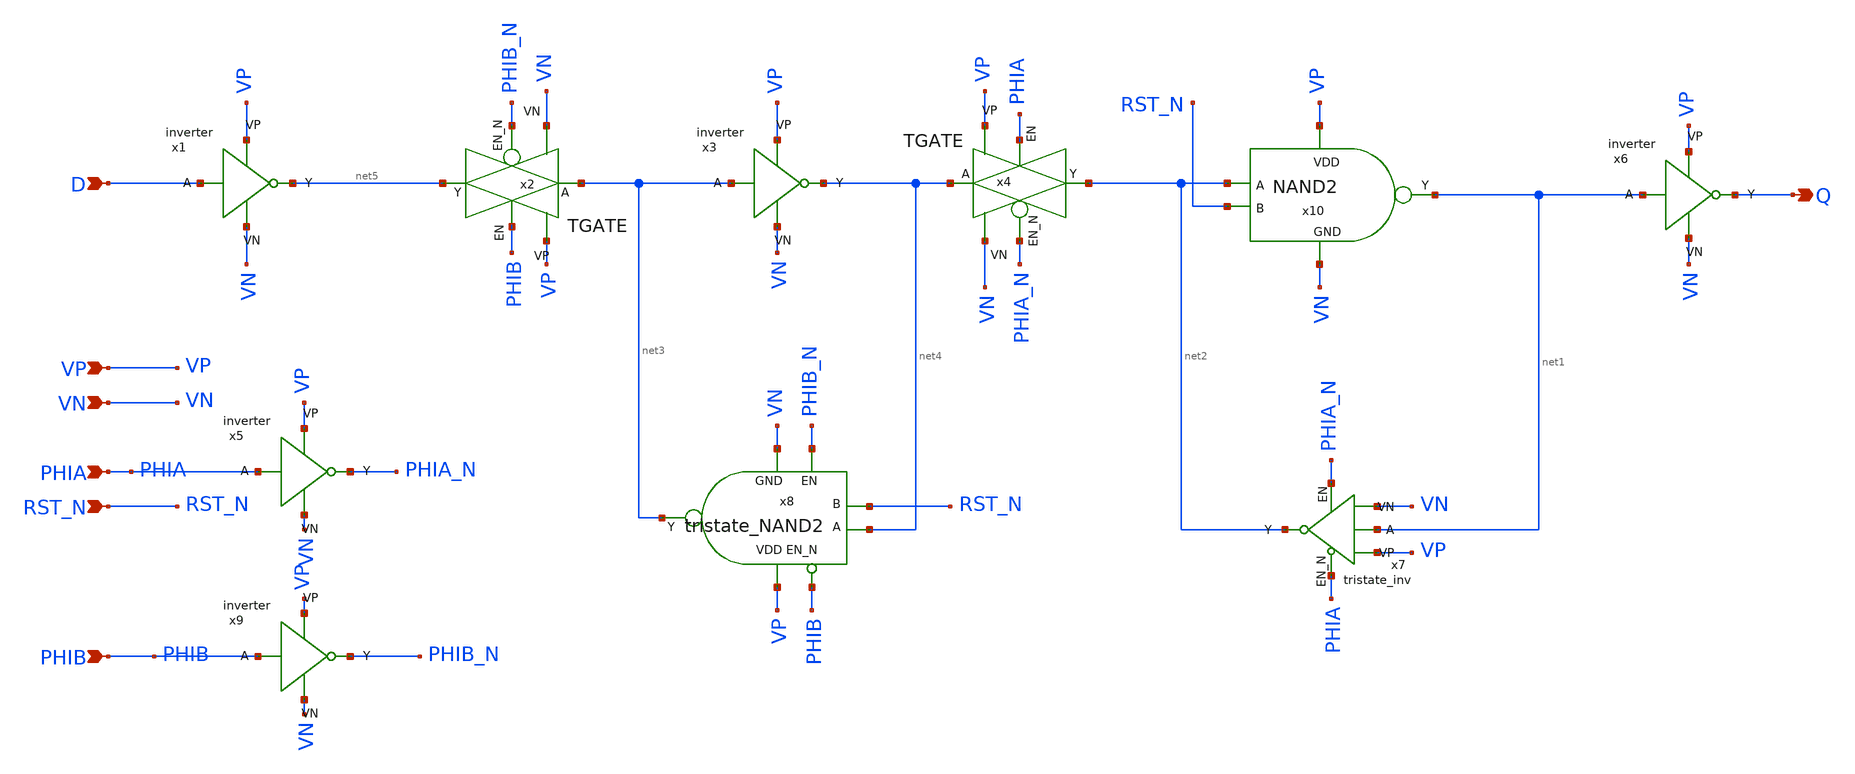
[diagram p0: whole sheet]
** sch_path: ADC/4bit_C2C/MagicAndSpice/EE431_FinalProj/DFFRN.sch
**.subckt DFFRN Q D VN RST_N VP PHIB PHIA
*.opin Q
*.ipin D
*.ipin VN
*.ipin RST_N
*.ipin VP
*.ipin PHIB
*.ipin PHIA
x1 D net5 VP VN inverter
x2 net3 net5 PHIB PHIB_N VP VN TGATE
x3 net3 net4 VP VN inverter
x4 net4 net2 PHIA PHIA_N VP VN TGATE
x6 net1 Q VP VN inverter
x7 net1 net2 PHIA_N PHIA VP VN tristate_inv
x8 net4 RST_N net3 PHIB_N PHIB VP VN tristate_NAND2
x10 VP net1 net2 RST_N VN NAND2
x5 PHIA PHIA_N VP VN inverter
x9 PHIB PHIB_N VP VN inverter
**.ends
.end
